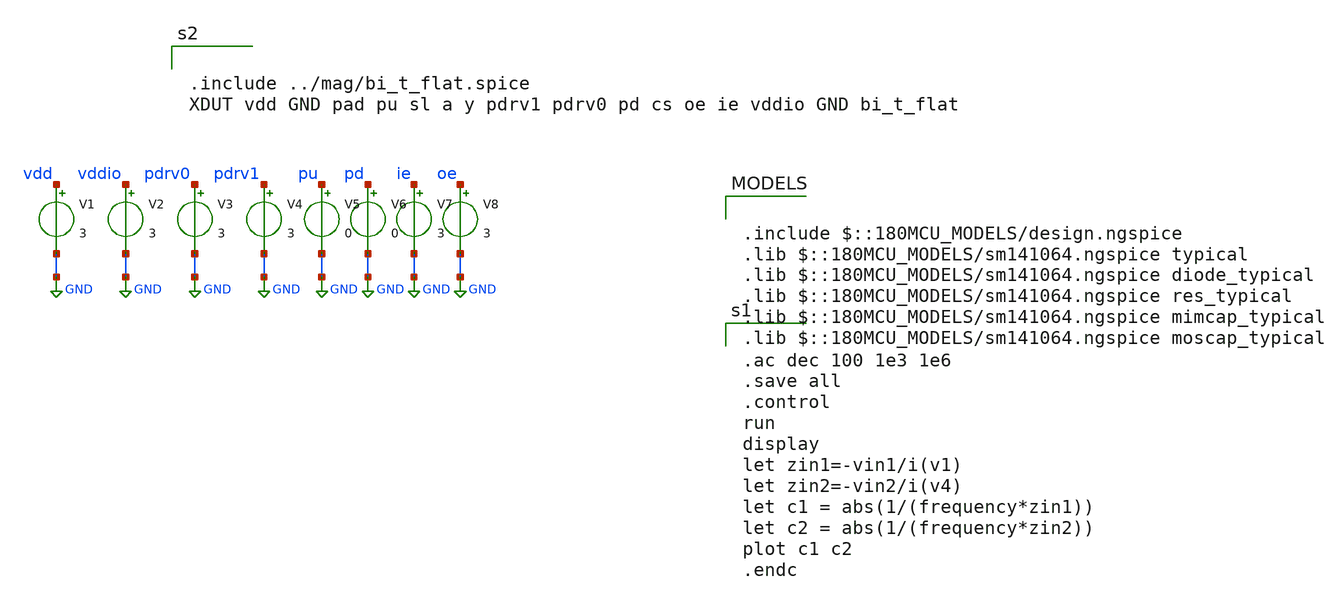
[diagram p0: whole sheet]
** sch_path: xschem/iotest_bi_t_pex.sch
**.subckt iotest_bi_t_pex
V1 vdd GND 3
V2 vddio GND 3
V3 pdrv0 GND 3
V4 pdrv1 GND 3
V5 pu GND 0
V6 pd GND 0
V7 ie GND 3
V8 oe GND 3
**** begin user architecture code


.ac dec 100 1e3 1e6
.save all
.control
run
display
let zin1=-vin1/i(v1)
let zin2=-vin2/i(v4)
let c1 = abs(1/(frequency*zin1))
let c2 = abs(1/(frequency*zin2))
plot c1 c2
.endc



.include $::180MCU_MODELS/design.ngspice
.lib $::180MCU_MODELS/sm141064.ngspice typical
.lib $::180MCU_MODELS/sm141064.ngspice diode_typical
.lib $::180MCU_MODELS/sm141064.ngspice res_typical
.lib $::180MCU_MODELS/sm141064.ngspice mimcap_typical
.lib $::180MCU_MODELS/sm141064.ngspice moscap_typical



.include ../mag/bi_t_flat.spice
XDUT vdd GND pad pu sl a y pdrv1 pdrv0 pd cs oe ie vddio GND bi_t_flat


**** end user architecture code
**.ends
.GLOBAL GND
.end
